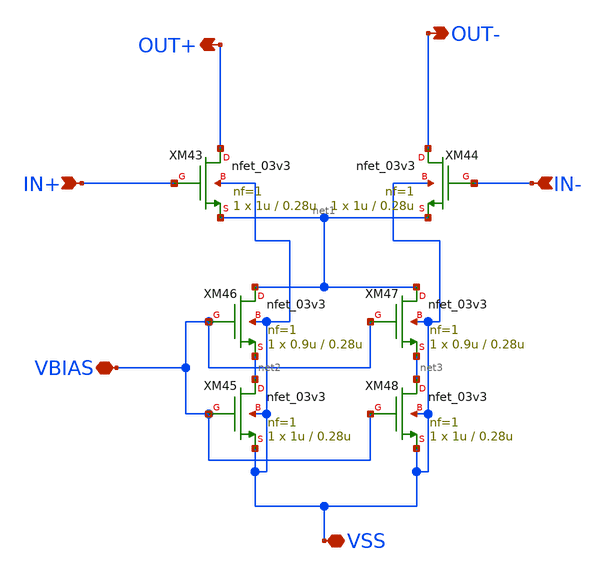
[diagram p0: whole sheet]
** sch_path: xschem/CS_Switch_16x.sch
**.subckt CS_Switch_16x IN+ IN- OUT+ OUT- VBIAS VSS
*.ipin IN+
*.ipin IN-
*.opin OUT+
*.opin OUT-
*.iopin VBIAS
*.iopin VSS
XM43 OUT+ IN+ net1 VSS nfet_03v3 L=0.28u W=1u nf=1 ad='int((nf+1)/2) * W/nf * 0.18u' as='int((nf+2)/2) * W/nf * 0.18u'
+ pd='2*int((nf+1)/2) * (W/nf + 0.18u)' ps='2*int((nf+2)/2) * (W/nf + 0.18u)' nrd='0.18u / W' nrs='0.18u / W'
+ sa=0 sb=0 sd=0 m=1
XM44 OUT- IN- net1 VSS nfet_03v3 L=0.28u W=1u nf=1 ad='int((nf+1)/2) * W/nf * 0.18u' as='int((nf+2)/2) * W/nf * 0.18u'
+ pd='2*int((nf+1)/2) * (W/nf + 0.18u)' ps='2*int((nf+2)/2) * (W/nf + 0.18u)' nrd='0.18u / W' nrs='0.18u / W'
+ sa=0 sb=0 sd=0 m=1
XM45 net2 VBIAS VSS VSS nfet_03v3 L=0.28u W=1u nf=1 ad='int((nf+1)/2) * W/nf * 0.18u' as='int((nf+2)/2) * W/nf * 0.18u'
+ pd='2*int((nf+1)/2) * (W/nf + 0.18u)' ps='2*int((nf+2)/2) * (W/nf + 0.18u)' nrd='0.18u / W' nrs='0.18u / W'
+ sa=0 sb=0 sd=0 m=1
XM46 net1 VBIAS net2 VSS nfet_03v3 L=0.28u W=0.9u nf=1 ad='int((nf+1)/2) * W/nf * 0.18u' as='int((nf+2)/2) * W/nf * 0.18u'
+ pd='2*int((nf+1)/2) * (W/nf + 0.18u)' ps='2*int((nf+2)/2) * (W/nf + 0.18u)' nrd='0.18u / W' nrs='0.18u / W'
+ sa=0 sb=0 sd=0 m=1
XM48 net3 VBIAS VSS VSS nfet_03v3 L=0.28u W=1u nf=1 ad='int((nf+1)/2) * W/nf * 0.18u' as='int((nf+2)/2) * W/nf * 0.18u'
+ pd='2*int((nf+1)/2) * (W/nf + 0.18u)' ps='2*int((nf+2)/2) * (W/nf + 0.18u)' nrd='0.18u / W' nrs='0.18u / W'
+ sa=0 sb=0 sd=0 m=1
XM47 net1 VBIAS net3 VSS nfet_03v3 L=0.28u W=0.9u nf=1 ad='int((nf+1)/2) * W/nf * 0.18u' as='int((nf+2)/2) * W/nf * 0.18u'
+ pd='2*int((nf+1)/2) * (W/nf + 0.18u)' ps='2*int((nf+2)/2) * (W/nf + 0.18u)' nrd='0.18u / W' nrs='0.18u / W'
+ sa=0 sb=0 sd=0 m=1
**.ends
.end
